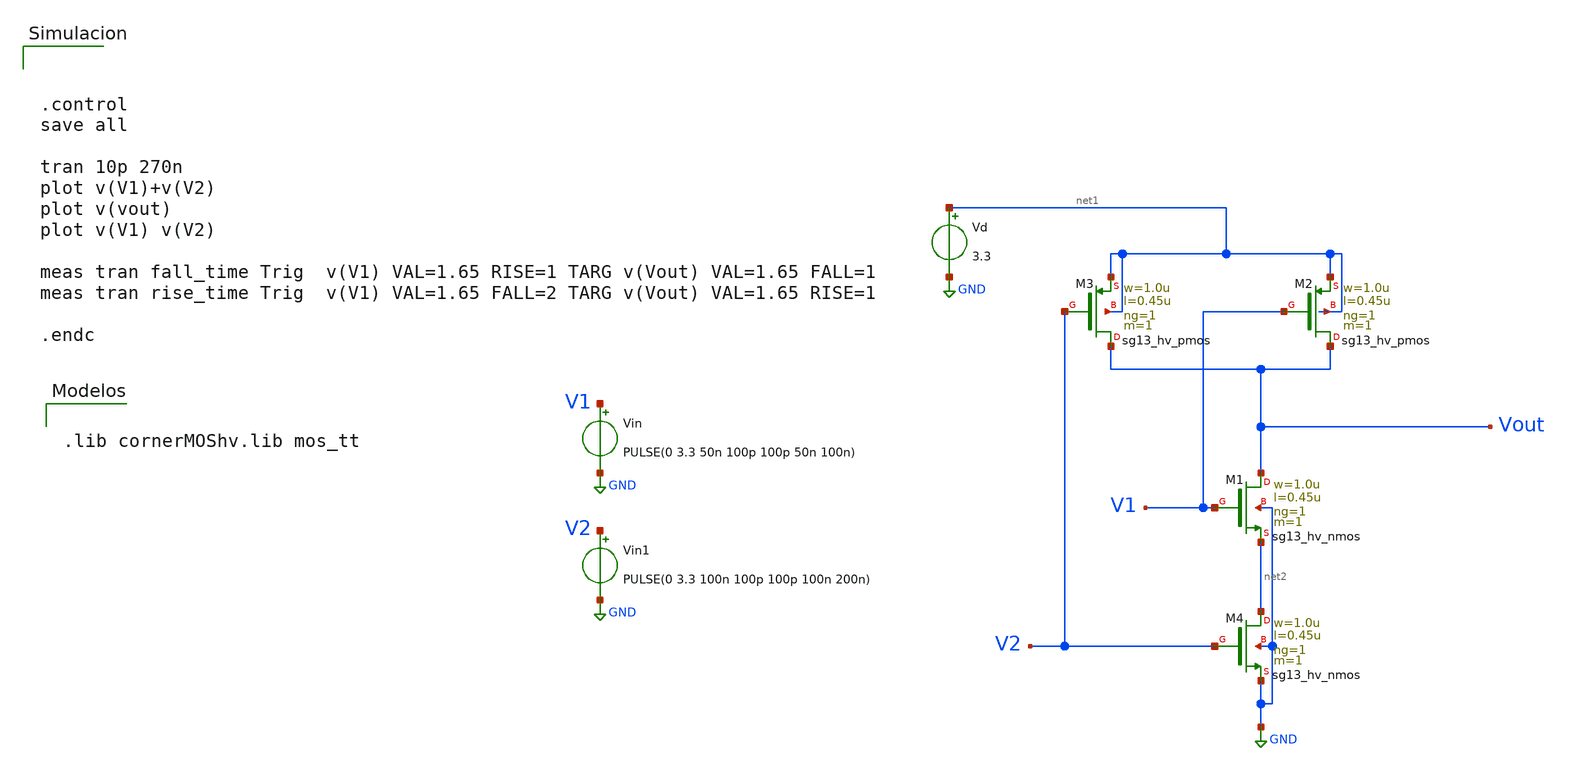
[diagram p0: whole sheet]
** sch_path: Taller2/Resuelto/nand_sim.sch
**.subckt nand_sim
XM1 Vout V1 net2 GND sg13_hv_nmos w=1.0u l=0.45u ng=1 m=1 mm_ok=1
XM2 Vout V1 net1 net1 sg13_hv_pmos w=1.0u l=0.45u ng=1 m=1 mm_ok=1
XM3 Vout V2 net1 net1 sg13_hv_pmos w=1.0u l=0.45u ng=1 m=1 mm_ok=1
XM4 net2 V2 GND GND sg13_hv_nmos w=1.0u l=0.45u ng=1 m=1 mm_ok=1
Vd net1 GND 3.3
Vin V1 GND PULSE(0 3.3 50n 100p 100p 50n 100n)
Vin1 V2 GND PULSE(0 3.3 100n 100p 100p 100n 200n)
**** begin user architecture code



.control
save all

tran 10p 270n
plot v(V1)+v(V2)
plot v(vout)
plot v(V1) v(V2)

meas tran fall_time Trig  v(V1) VAL=1.65 RISE=1 TARG v(Vout) VAL=1.65 FALL=1
meas tran rise_time Trig  v(V1) VAL=1.65 FALL=2 TARG v(Vout) VAL=1.65 RISE=1

.endc




.lib cornerMOShv.lib mos_tt


**** end user architecture code
**.ends
.GLOBAL GND
.end
